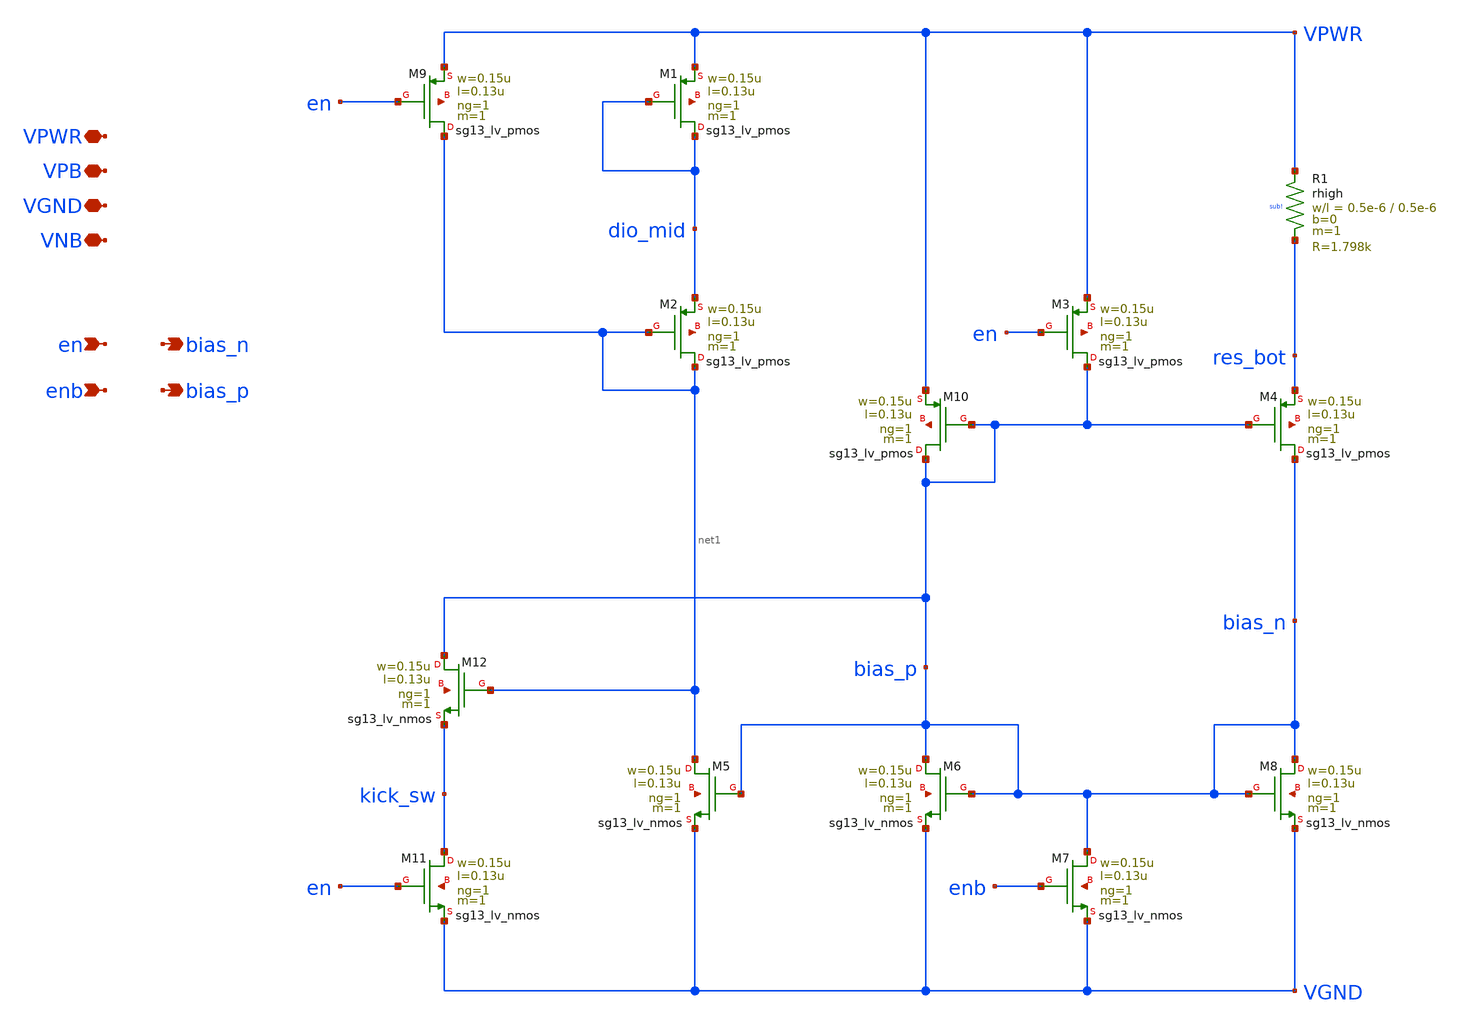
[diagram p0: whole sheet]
** sch_path: Team 2 Design/design_data/xschem/t2_bias.sch
**.subckt t2_bias VPWR VPB VGND VNB en enb bias_n bias_p
*.iopin VPWR
*.iopin VPB
*.iopin VGND
*.iopin VNB
*.ipin en
*.ipin enb
*.opin bias_n
*.opin bias_p
XM9 net1 en VPWR net2 sg13_lv_pmos w=0.15u l=0.13u ng=1 m=1 mm_ok=1
XM10 bias_p bias_p VPWR net3 sg13_lv_pmos w=0.15u l=0.13u ng=1 m=1 mm_ok=1
XM1 dio_mid dio_mid VPWR net4 sg13_lv_pmos w=0.15u l=0.13u ng=1 m=1 mm_ok=1
XM2 net1 net1 dio_mid net5 sg13_lv_pmos w=0.15u l=0.13u ng=1 m=1 mm_ok=1
XM3 bias_p en VPWR net6 sg13_lv_pmos w=0.15u l=0.13u ng=1 m=1 mm_ok=1
XM4 bias_p bias_p res_bot net7 sg13_lv_pmos w=0.15u l=0.13u ng=1 m=1 mm_ok=1
XM11 kick_sw en VGND net8 sg13_lv_nmos w=0.15u l=0.13u ng=1 m=1 mm_ok=1
XM12 bias_p net1 kick_sw net9 sg13_lv_nmos w=0.15u l=0.13u ng=1 m=1 mm_ok=1
XM5 net1 bias_p VGND net10 sg13_lv_nmos w=0.15u l=0.13u ng=1 m=1 mm_ok=1
XM6 bias_p bias_p VGND net11 sg13_lv_nmos w=0.15u l=0.13u ng=1 m=1 mm_ok=1
XM7 bias_p enb VGND net12 sg13_lv_nmos w=0.15u l=0.13u ng=1 m=1 mm_ok=1
XM8 bias_p bias_p VGND net13 sg13_lv_nmos w=0.15u l=0.13u ng=1 m=1 mm_ok=1
XR1 VPWR res_bot sub! rhigh w=0.5e-6 l=0.5e-6 m=1 b=0 mm_ok=1
**.ends
.end
